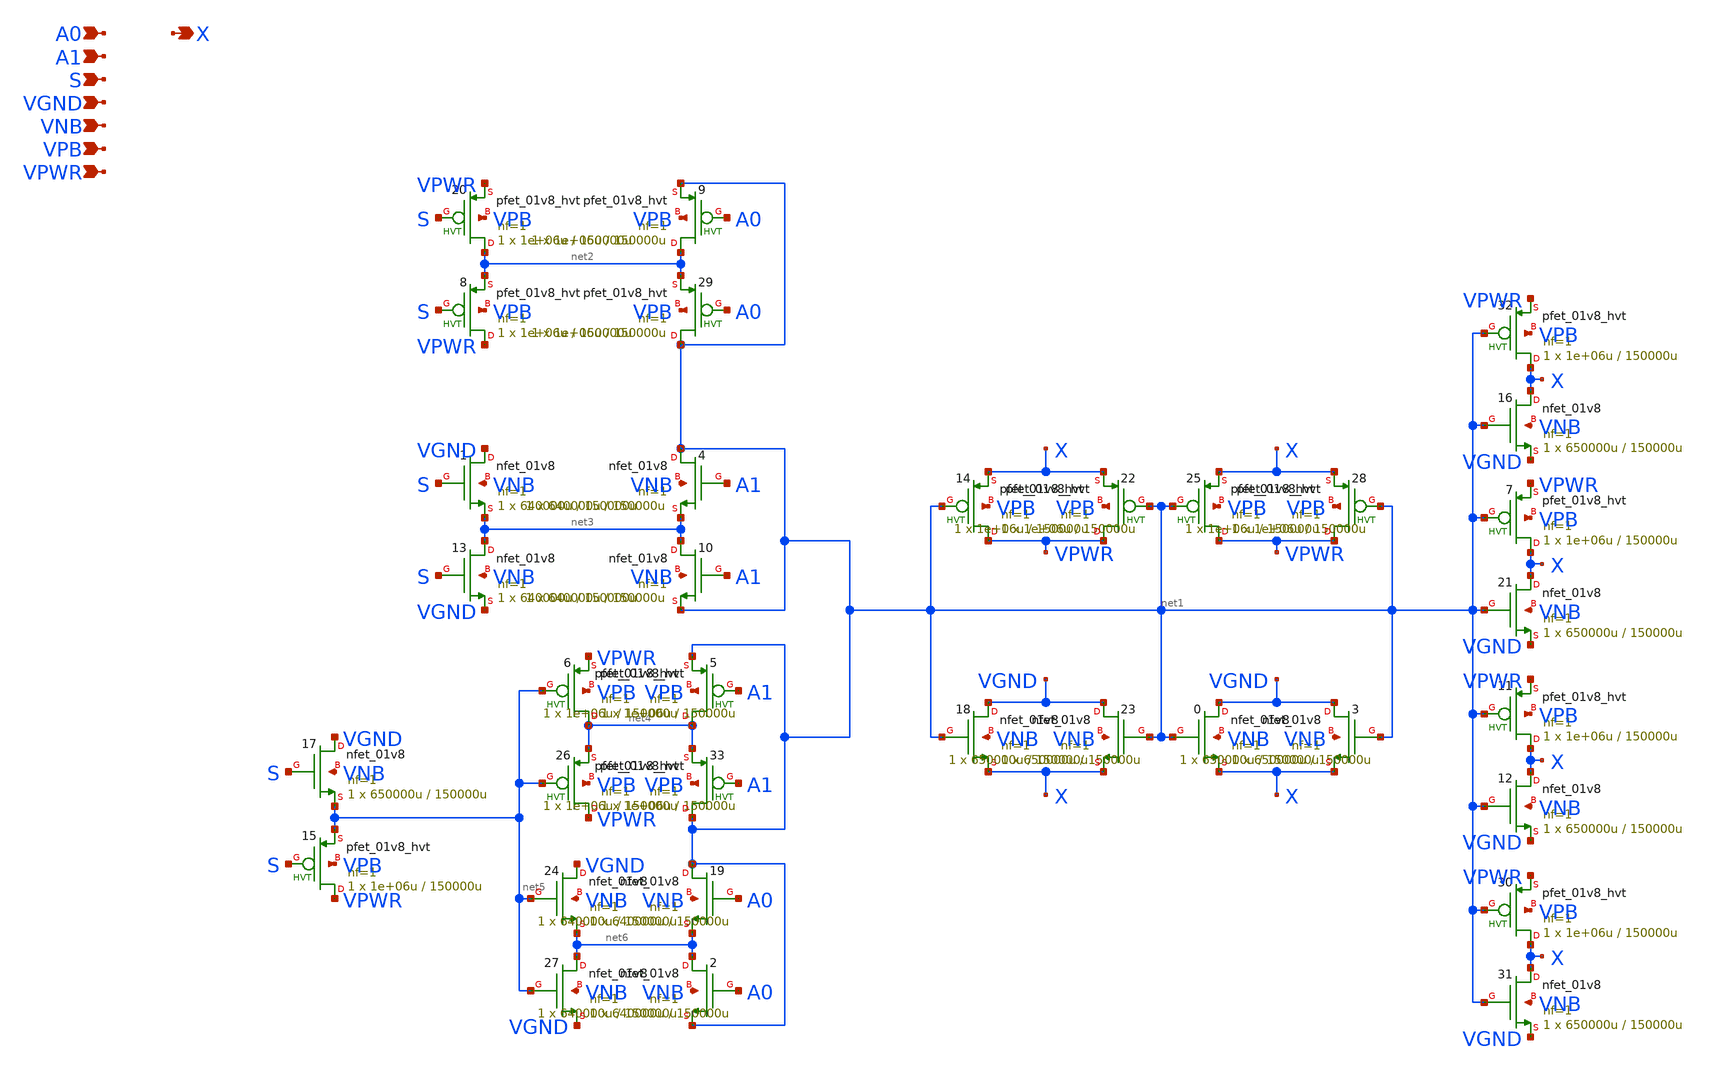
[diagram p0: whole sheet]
** sch_path: schematics/mux2/sky130_fd_sc_hd__mux2_8.sch
**.subckt sky130_fd_sc_hd__mux2_8 A0 A1 S VGND VNB VPB VPWR X
*.ipin A0
*.ipin A1
*.ipin S
*.ipin VGND
*.ipin VNB
*.ipin VPB
*.ipin VPWR
*.opin X
X0 VGND net1 X VNB sky130_fd_pr__nfet_01v8 L=150000u W=650000u nf=1 ad='int((1 + 1)/2) * 650000u / 1 * 0.29'
+ as='int((1 + 2)/2) * 650000u / 1 * 0.29' pd='2*int((1 + 1)/2) * (650000u / 1 + 0.29)' ps='2*int((1 + 2)/2) * (650000u / 1 + 0.29)'
+ nrd='0.29 / 650000u ' nrs='0.29 / 650000u ' sa=0 sb=0 sd=0 mult=1 m=1
X11 X net1 VPWR VPB sky130_fd_pr__pfet_01v8_hvt L=150000u W=1e+06u nf=1 ad='int((1 + 1)/2) * 1e+06u / 1 * 0.29'
+ as='int((1 + 2)/2) * 1e+06u / 1 * 0.29' pd='2*int((1 + 1)/2) * (1e+06u / 1 + 0.29)' ps='2*int((1 + 2)/2) * (1e+06u / 1 + 0.29)'
+ nrd='0.29 / 1e+06u ' nrs='0.29 / 1e+06u ' sa=0 sb=0 sd=0 mult=1 m=1
X12 X net1 VGND VNB sky130_fd_pr__nfet_01v8 L=150000u W=650000u nf=1 ad='int((1 + 1)/2) * 650000u / 1 * 0.29'
+ as='int((1 + 2)/2) * 650000u / 1 * 0.29' pd='2*int((1 + 1)/2) * (650000u / 1 + 0.29)' ps='2*int((1 + 2)/2) * (650000u / 1 + 0.29)'
+ nrd='0.29 / 650000u ' nrs='0.29 / 650000u ' sa=0 sb=0 sd=0 mult=1 m=1
X3 VGND net1 X VNB sky130_fd_pr__nfet_01v8 L=150000u W=650000u nf=1 ad='int((1 + 1)/2) * 650000u / 1 * 0.29'
+ as='int((1 + 2)/2) * 650000u / 1 * 0.29' pd='2*int((1 + 1)/2) * (650000u / 1 + 0.29)' ps='2*int((1 + 2)/2) * (650000u / 1 + 0.29)'
+ nrd='0.29 / 650000u ' nrs='0.29 / 650000u ' sa=0 sb=0 sd=0 mult=1 m=1
X7 X net1 VPWR VPB sky130_fd_pr__pfet_01v8_hvt L=150000u W=1e+06u nf=1 ad='int((1 + 1)/2) * 1e+06u / 1 * 0.29'
+ as='int((1 + 2)/2) * 1e+06u / 1 * 0.29' pd='2*int((1 + 1)/2) * (1e+06u / 1 + 0.29)' ps='2*int((1 + 2)/2) * (1e+06u / 1 + 0.29)'
+ nrd='0.29 / 1e+06u ' nrs='0.29 / 1e+06u ' sa=0 sb=0 sd=0 mult=1 m=1
X30 X net1 VPWR VPB sky130_fd_pr__pfet_01v8_hvt L=150000u W=1e+06u nf=1 ad='int((1 + 1)/2) * 1e+06u / 1 * 0.29'
+ as='int((1 + 2)/2) * 1e+06u / 1 * 0.29' pd='2*int((1 + 1)/2) * (1e+06u / 1 + 0.29)' ps='2*int((1 + 2)/2) * (1e+06u / 1 + 0.29)'
+ nrd='0.29 / 1e+06u ' nrs='0.29 / 1e+06u ' sa=0 sb=0 sd=0 mult=1 m=1
X16 X net1 VGND VNB sky130_fd_pr__nfet_01v8 L=150000u W=650000u nf=1 ad='int((1 + 1)/2) * 650000u / 1 * 0.29'
+ as='int((1 + 2)/2) * 650000u / 1 * 0.29' pd='2*int((1 + 1)/2) * (650000u / 1 + 0.29)' ps='2*int((1 + 2)/2) * (650000u / 1 + 0.29)'
+ nrd='0.29 / 650000u ' nrs='0.29 / 650000u ' sa=0 sb=0 sd=0 mult=1 m=1
X21 X net1 VGND VNB sky130_fd_pr__nfet_01v8 L=150000u W=650000u nf=1 ad='int((1 + 1)/2) * 650000u / 1 * 0.29'
+ as='int((1 + 2)/2) * 650000u / 1 * 0.29' pd='2*int((1 + 1)/2) * (650000u / 1 + 0.29)' ps='2*int((1 + 2)/2) * (650000u / 1 + 0.29)'
+ nrd='0.29 / 650000u ' nrs='0.29 / 650000u ' sa=0 sb=0 sd=0 mult=1 m=1
X31 X net1 VGND VNB sky130_fd_pr__nfet_01v8 L=150000u W=650000u nf=1 ad='int((1 + 1)/2) * 650000u / 1 * 0.29'
+ as='int((1 + 2)/2) * 650000u / 1 * 0.29' pd='2*int((1 + 1)/2) * (650000u / 1 + 0.29)' ps='2*int((1 + 2)/2) * (650000u / 1 + 0.29)'
+ nrd='0.29 / 650000u ' nrs='0.29 / 650000u ' sa=0 sb=0 sd=0 mult=1 m=1
X32 X net1 VPWR VPB sky130_fd_pr__pfet_01v8_hvt L=150000u W=1e+06u nf=1 ad='int((1 + 1)/2) * 1e+06u / 1 * 0.29'
+ as='int((1 + 2)/2) * 1e+06u / 1 * 0.29' pd='2*int((1 + 1)/2) * (1e+06u / 1 + 0.29)' ps='2*int((1 + 2)/2) * (1e+06u / 1 + 0.29)'
+ nrd='0.29 / 1e+06u ' nrs='0.29 / 1e+06u ' sa=0 sb=0 sd=0 mult=1 m=1
X18 VGND net1 X VNB sky130_fd_pr__nfet_01v8 L=150000u W=650000u nf=1 ad='int((1 + 1)/2) * 650000u / 1 * 0.29'
+ as='int((1 + 2)/2) * 650000u / 1 * 0.29' pd='2*int((1 + 1)/2) * (650000u / 1 + 0.29)' ps='2*int((1 + 2)/2) * (650000u / 1 + 0.29)'
+ nrd='0.29 / 650000u ' nrs='0.29 / 650000u ' sa=0 sb=0 sd=0 mult=1 m=1
X23 VGND net1 X VNB sky130_fd_pr__nfet_01v8 L=150000u W=650000u nf=1 ad='int((1 + 1)/2) * 650000u / 1 * 0.29'
+ as='int((1 + 2)/2) * 650000u / 1 * 0.29' pd='2*int((1 + 1)/2) * (650000u / 1 + 0.29)' ps='2*int((1 + 2)/2) * (650000u / 1 + 0.29)'
+ nrd='0.29 / 650000u ' nrs='0.29 / 650000u ' sa=0 sb=0 sd=0 mult=1 m=1
X14 VPWR net1 X VPB sky130_fd_pr__pfet_01v8_hvt L=150000u W=1e+06u nf=1 ad='int((1 + 1)/2) * 1e+06u / 1 * 0.29'
+ as='int((1 + 2)/2) * 1e+06u / 1 * 0.29' pd='2*int((1 + 1)/2) * (1e+06u / 1 + 0.29)' ps='2*int((1 + 2)/2) * (1e+06u / 1 + 0.29)'
+ nrd='0.29 / 1e+06u ' nrs='0.29 / 1e+06u ' sa=0 sb=0 sd=0 mult=1 m=1
X22 VPWR net1 X VPB sky130_fd_pr__pfet_01v8_hvt L=150000u W=1e+06u nf=1 ad='int((1 + 1)/2) * 1e+06u / 1 * 0.29'
+ as='int((1 + 2)/2) * 1e+06u / 1 * 0.29' pd='2*int((1 + 1)/2) * (1e+06u / 1 + 0.29)' ps='2*int((1 + 2)/2) * (1e+06u / 1 + 0.29)'
+ nrd='0.29 / 1e+06u ' nrs='0.29 / 1e+06u ' sa=0 sb=0 sd=0 mult=1 m=1
X25 VPWR net1 X VPB sky130_fd_pr__pfet_01v8_hvt L=150000u W=1e+06u nf=1 ad='int((1 + 1)/2) * 1e+06u / 1 * 0.29'
+ as='int((1 + 2)/2) * 1e+06u / 1 * 0.29' pd='2*int((1 + 1)/2) * (1e+06u / 1 + 0.29)' ps='2*int((1 + 2)/2) * (1e+06u / 1 + 0.29)'
+ nrd='0.29 / 1e+06u ' nrs='0.29 / 1e+06u ' sa=0 sb=0 sd=0 mult=1 m=1
X28 VPWR net1 X VPB sky130_fd_pr__pfet_01v8_hvt L=150000u W=1e+06u nf=1 ad='int((1 + 1)/2) * 1e+06u / 1 * 0.29'
+ as='int((1 + 2)/2) * 1e+06u / 1 * 0.29' pd='2*int((1 + 1)/2) * (1e+06u / 1 + 0.29)' ps='2*int((1 + 2)/2) * (1e+06u / 1 + 0.29)'
+ nrd='0.29 / 1e+06u ' nrs='0.29 / 1e+06u ' sa=0 sb=0 sd=0 mult=1 m=1
X29 net1 A0 net2 VPB sky130_fd_pr__pfet_01v8_hvt L=150000u W=1e+06u nf=1 ad='int((1 + 1)/2) * 1e+06u / 1 * 0.29'
+ as='int((1 + 2)/2) * 1e+06u / 1 * 0.29' pd='2*int((1 + 1)/2) * (1e+06u / 1 + 0.29)' ps='2*int((1 + 2)/2) * (1e+06u / 1 + 0.29)'
+ nrd='0.29 / 1e+06u ' nrs='0.29 / 1e+06u ' sa=0 sb=0 sd=0 mult=1 m=1
X20 net2 S VPWR VPB sky130_fd_pr__pfet_01v8_hvt L=150000u W=1e+06u nf=1 ad='int((1 + 1)/2) * 1e+06u / 1 * 0.29'
+ as='int((1 + 2)/2) * 1e+06u / 1 * 0.29' pd='2*int((1 + 1)/2) * (1e+06u / 1 + 0.29)' ps='2*int((1 + 2)/2) * (1e+06u / 1 + 0.29)'
+ nrd='0.29 / 1e+06u ' nrs='0.29 / 1e+06u ' sa=0 sb=0 sd=0 mult=1 m=1
X8 VPWR S net2 VPB sky130_fd_pr__pfet_01v8_hvt L=150000u W=1e+06u nf=1 ad='int((1 + 1)/2) * 1e+06u / 1 * 0.29'
+ as='int((1 + 2)/2) * 1e+06u / 1 * 0.29' pd='2*int((1 + 1)/2) * (1e+06u / 1 + 0.29)' ps='2*int((1 + 2)/2) * (1e+06u / 1 + 0.29)'
+ nrd='0.29 / 1e+06u ' nrs='0.29 / 1e+06u ' sa=0 sb=0 sd=0 mult=1 m=1
X9 net2 A0 net1 VPB sky130_fd_pr__pfet_01v8_hvt L=150000u W=1e+06u nf=1 ad='int((1 + 1)/2) * 1e+06u / 1 * 0.29'
+ as='int((1 + 2)/2) * 1e+06u / 1 * 0.29' pd='2*int((1 + 1)/2) * (1e+06u / 1 + 0.29)' ps='2*int((1 + 2)/2) * (1e+06u / 1 + 0.29)'
+ nrd='0.29 / 1e+06u ' nrs='0.29 / 1e+06u ' sa=0 sb=0 sd=0 mult=1 m=1
X1 VGND S net3 VNB sky130_fd_pr__nfet_01v8 L=150000u W=640000u nf=1 ad='int((1 + 1)/2) * 640000u / 1 * 0.29'
+ as='int((1 + 2)/2) * 640000u / 1 * 0.29' pd='2*int((1 + 1)/2) * (640000u / 1 + 0.29)' ps='2*int((1 + 2)/2) * (640000u / 1 + 0.29)'
+ nrd='0.29 / 640000u ' nrs='0.29 / 640000u ' sa=0 sb=0 sd=0 mult=1 m=1
X4 net1 A1 net3 VNB sky130_fd_pr__nfet_01v8 L=150000u W=640000u nf=1 ad='int((1 + 1)/2) * 640000u / 1 * 0.29'
+ as='int((1 + 2)/2) * 640000u / 1 * 0.29' pd='2*int((1 + 1)/2) * (640000u / 1 + 0.29)' ps='2*int((1 + 2)/2) * (640000u / 1 + 0.29)'
+ nrd='0.29 / 640000u ' nrs='0.29 / 640000u ' sa=0 sb=0 sd=0 mult=1 m=1
X10 net3 A1 net1 VNB sky130_fd_pr__nfet_01v8 L=150000u W=640000u nf=1 ad='int((1 + 1)/2) * 640000u / 1 * 0.29'
+ as='int((1 + 2)/2) * 640000u / 1 * 0.29' pd='2*int((1 + 1)/2) * (640000u / 1 + 0.29)' ps='2*int((1 + 2)/2) * (640000u / 1 + 0.29)'
+ nrd='0.29 / 640000u ' nrs='0.29 / 640000u ' sa=0 sb=0 sd=0 mult=1 m=1
X13 net3 S VGND VNB sky130_fd_pr__nfet_01v8 L=150000u W=640000u nf=1 ad='int((1 + 1)/2) * 640000u / 1 * 0.29'
+ as='int((1 + 2)/2) * 640000u / 1 * 0.29' pd='2*int((1 + 1)/2) * (640000u / 1 + 0.29)' ps='2*int((1 + 2)/2) * (640000u / 1 + 0.29)'
+ nrd='0.29 / 640000u ' nrs='0.29 / 640000u ' sa=0 sb=0 sd=0 mult=1 m=1
X2 net6 A0 net1 VNB sky130_fd_pr__nfet_01v8 L=150000u W=640000u nf=1 ad='int((1 + 1)/2) * 640000u / 1 * 0.29'
+ as='int((1 + 2)/2) * 640000u / 1 * 0.29' pd='2*int((1 + 1)/2) * (640000u / 1 + 0.29)' ps='2*int((1 + 2)/2) * (640000u / 1 + 0.29)'
+ nrd='0.29 / 640000u ' nrs='0.29 / 640000u ' sa=0 sb=0 sd=0 mult=1 m=1
X5 net4 A1 net1 VPB sky130_fd_pr__pfet_01v8_hvt L=150000u W=1e+06u nf=1 ad='int((1 + 1)/2) * 1e+06u / 1 * 0.29'
+ as='int((1 + 2)/2) * 1e+06u / 1 * 0.29' pd='2*int((1 + 1)/2) * (1e+06u / 1 + 0.29)' ps='2*int((1 + 2)/2) * (1e+06u / 1 + 0.29)'
+ nrd='0.29 / 1e+06u ' nrs='0.29 / 1e+06u ' sa=0 sb=0 sd=0 mult=1 m=1
X15 VPWR S net5 VPB sky130_fd_pr__pfet_01v8_hvt L=150000u W=1e+06u nf=1 ad='int((1 + 1)/2) * 1e+06u / 1 * 0.29'
+ as='int((1 + 2)/2) * 1e+06u / 1 * 0.29' pd='2*int((1 + 1)/2) * (1e+06u / 1 + 0.29)' ps='2*int((1 + 2)/2) * (1e+06u / 1 + 0.29)'
+ nrd='0.29 / 1e+06u ' nrs='0.29 / 1e+06u ' sa=0 sb=0 sd=0 mult=1 m=1
X17 VGND S net5 VNB sky130_fd_pr__nfet_01v8 L=150000u W=650000u nf=1 ad='int((1 + 1)/2) * 650000u / 1 * 0.29'
+ as='int((1 + 2)/2) * 650000u / 1 * 0.29' pd='2*int((1 + 1)/2) * (650000u / 1 + 0.29)' ps='2*int((1 + 2)/2) * (650000u / 1 + 0.29)'
+ nrd='0.29 / 650000u ' nrs='0.29 / 650000u ' sa=0 sb=0 sd=0 mult=1 m=1
X24 VGND net5 net6 VNB sky130_fd_pr__nfet_01v8 L=150000u W=640000u nf=1 ad='int((1 + 1)/2) * 640000u / 1 * 0.29'
+ as='int((1 + 2)/2) * 640000u / 1 * 0.29' pd='2*int((1 + 1)/2) * (640000u / 1 + 0.29)' ps='2*int((1 + 2)/2) * (640000u / 1 + 0.29)'
+ nrd='0.29 / 640000u ' nrs='0.29 / 640000u ' sa=0 sb=0 sd=0 mult=1 m=1
X26 VPWR net5 net4 VPB sky130_fd_pr__pfet_01v8_hvt L=150000u W=1e+06u nf=1 ad='int((1 + 1)/2) * 1e+06u / 1 * 0.29'
+ as='int((1 + 2)/2) * 1e+06u / 1 * 0.29' pd='2*int((1 + 1)/2) * (1e+06u / 1 + 0.29)' ps='2*int((1 + 2)/2) * (1e+06u / 1 + 0.29)'
+ nrd='0.29 / 1e+06u ' nrs='0.29 / 1e+06u ' sa=0 sb=0 sd=0 mult=1 m=1
X27 net6 net5 VGND VNB sky130_fd_pr__nfet_01v8 L=150000u W=640000u nf=1 ad='int((1 + 1)/2) * 640000u / 1 * 0.29'
+ as='int((1 + 2)/2) * 640000u / 1 * 0.29' pd='2*int((1 + 1)/2) * (640000u / 1 + 0.29)' ps='2*int((1 + 2)/2) * (640000u / 1 + 0.29)'
+ nrd='0.29 / 640000u ' nrs='0.29 / 640000u ' sa=0 sb=0 sd=0 mult=1 m=1
X33 net1 A1 net4 VPB sky130_fd_pr__pfet_01v8_hvt L=150000u W=1e+06u nf=1 ad='int((1 + 1)/2) * 1e+06u / 1 * 0.29'
+ as='int((1 + 2)/2) * 1e+06u / 1 * 0.29' pd='2*int((1 + 1)/2) * (1e+06u / 1 + 0.29)' ps='2*int((1 + 2)/2) * (1e+06u / 1 + 0.29)'
+ nrd='0.29 / 1e+06u ' nrs='0.29 / 1e+06u ' sa=0 sb=0 sd=0 mult=1 m=1
X6 net4 net5 VPWR VPB sky130_fd_pr__pfet_01v8_hvt L=150000u W=1e+06u nf=1 ad='int((1 + 1)/2) * 1e+06u / 1 * 0.29'
+ as='int((1 + 2)/2) * 1e+06u / 1 * 0.29' pd='2*int((1 + 1)/2) * (1e+06u / 1 + 0.29)' ps='2*int((1 + 2)/2) * (1e+06u / 1 + 0.29)'
+ nrd='0.29 / 1e+06u ' nrs='0.29 / 1e+06u ' sa=0 sb=0 sd=0 mult=1 m=1
X19 net1 A0 net6 VNB sky130_fd_pr__nfet_01v8 L=150000u W=640000u nf=1 ad='int((1 + 1)/2) * 640000u / 1 * 0.29'
+ as='int((1 + 2)/2) * 640000u / 1 * 0.29' pd='2*int((1 + 1)/2) * (640000u / 1 + 0.29)' ps='2*int((1 + 2)/2) * (640000u / 1 + 0.29)'
+ nrd='0.29 / 640000u ' nrs='0.29 / 640000u ' sa=0 sb=0 sd=0 mult=1 m=1
**.ends
.end
